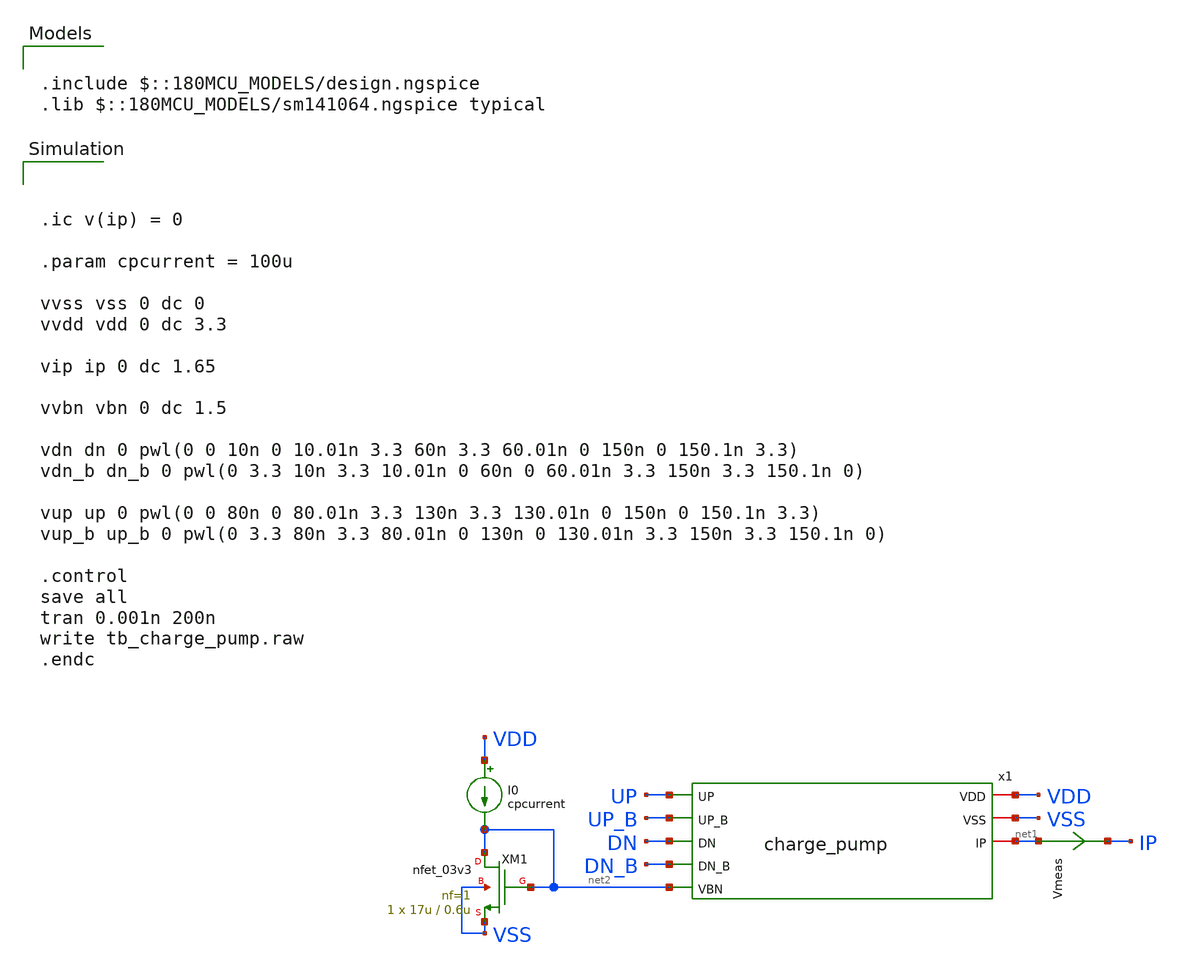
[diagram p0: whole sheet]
** sch_path: designs/libs/tb_analog/tb_charge_pump/tb_charge_pump.sch
**.subckt tb_charge_pump
x1 VDD VSS UP UP_B DN DN_B net2 net1 charge_pump
Vmeas net1 IP 0
.save i(vmeas)
XM1 net2 net2 VSS VSS nfet_03v3 L=0.6u W=17u nf=1 ad='int((nf+1)/2) * W/nf * 0.18u' as='int((nf+2)/2) * W/nf * 0.18u'
+ pd='2*int((nf+1)/2) * (W/nf + 0.18u)' ps='2*int((nf+2)/2) * (W/nf + 0.18u)' nrd='0.18u / W' nrs='0.18u / W'
+ sa=0 sb=0 sd=0 m=1
I0 VDD net2 cpcurrent
**** begin user architecture code



.ic v(ip) = 0

.param cpcurrent = 100u

vvss vss 0 dc 0
vvdd vdd 0 dc 3.3

vip ip 0 dc 1.65

vvbn vbn 0 dc 1.5

vdn dn 0 pwl(0 0 10n 0 10.01n 3.3 60n 3.3 60.01n 0 150n 0 150.1n 3.3)
vdn_b dn_b 0 pwl(0 3.3 10n 3.3 10.01n 0 60n 0 60.01n 3.3 150n 3.3 150.1n 0)

vup up 0 pwl(0 0 80n 0 80.01n 3.3 130n 3.3 130.01n 0 150n 0 150.1n 3.3)
vup_b up_b 0 pwl(0 3.3 80n 3.3 80.01n 0 130n 0 130.01n 3.3 150n 3.3 150.1n 0)

.control
save all
tran 0.001n 200n
write tb_charge_pump.raw
.endc



.include $::180MCU_MODELS/design.ngspice
.lib $::180MCU_MODELS/sm141064.ngspice typical

**** end user architecture code
**.ends

* expanding   symbol:
*+  /foss/designs/synchronos-chipathon-2026/designs/libs/core_analog/charge_pump/charge_pump.sym # of pins=8
** sym_path: designs/libs/core_analog/charge_pump/charge_pump.sym
** sch_path: designs/libs/core_analog/charge_pump/charge_pump.sch
.subckt charge_pump VDD VSS UP UP_B DN DN_B VBN IP
*.iopin VDD
*.iopin VSS
*.ipin UP
*.ipin UP_B
*.ipin DN
*.ipin DN_B
*.ipin VBN
*.iopin IP
XM1 net1 VBN net7 VSS nfet_03v3 L=0.6u W=17u nf=1 ad='int((nf+1)/2) * W/nf * 0.18u' as='int((nf+2)/2) * W/nf * 0.18u'
+ pd='2*int((nf+1)/2) * (W/nf + 0.18u)' ps='2*int((nf+2)/2) * (W/nf + 0.18u)' nrd='0.18u / W' nrs='0.18u / W'
+ sa=0 sb=0 sd=0 m=1
XM2 net2 VBN net6 VSS nfet_03v3 L=0.6u W=17u nf=1 ad='int((nf+1)/2) * W/nf * 0.18u' as='int((nf+2)/2) * W/nf * 0.18u'
+ pd='2*int((nf+1)/2) * (W/nf + 0.18u)' ps='2*int((nf+2)/2) * (W/nf + 0.18u)' nrd='0.18u / W' nrs='0.18u / W'
+ sa=0 sb=0 sd=0 m=1
XM3 net5 DN net1 VSS nfet_03v3 L=0.3u W=1.5u nf=1 ad='int((nf+1)/2) * W/nf * 0.18u' as='int((nf+2)/2) * W/nf * 0.18u'
+ pd='2*int((nf+1)/2) * (W/nf + 0.18u)' ps='2*int((nf+2)/2) * (W/nf + 0.18u)' nrd='0.18u / W' nrs='0.18u / W'
+ sa=0 sb=0 sd=0 m=1
XM4 net3 DN_B net1 VSS nfet_03v3 L=0.3u W=1.5u nf=1 ad='int((nf+1)/2) * W/nf * 0.18u' as='int((nf+2)/2) * W/nf * 0.18u'
+ pd='2*int((nf+1)/2) * (W/nf + 0.18u)' ps='2*int((nf+2)/2) * (W/nf + 0.18u)' nrd='0.18u / W' nrs='0.18u / W'
+ sa=0 sb=0 sd=0 m=1
XM5 net4 UP_B net2 VSS nfet_03v3 L=0.3u W=1.5u nf=1 ad='int((nf+1)/2) * W/nf * 0.18u' as='int((nf+2)/2) * W/nf * 0.18u'
+ pd='2*int((nf+1)/2) * (W/nf + 0.18u)' ps='2*int((nf+2)/2) * (W/nf + 0.18u)' nrd='0.18u / W' nrs='0.18u / W'
+ sa=0 sb=0 sd=0 m=1
XM6 IP UP net2 VSS nfet_03v3 L=0.3u W=1.5u nf=1 ad='int((nf+1)/2) * W/nf * 0.18u' as='int((nf+2)/2) * W/nf * 0.18u'
+ pd='2*int((nf+1)/2) * (W/nf + 0.18u)' ps='2*int((nf+2)/2) * (W/nf + 0.18u)' nrd='0.18u / W' nrs='0.18u / W'
+ sa=0 sb=0 sd=0 m=1
x1 net5 net5 VDD net5 VDD cp_sym_load
x2 net3 net3 VDD net3 VDD cp_sym_load
x3 net4 net4 VDD net4 VDD cp_sym_load
x4 net5 net5 VDD IP VDD cp_sym_load
Vtail net7 VSS 0
.save i(vtail)
Vtail2 net6 VSS 0
.save i(vtail2)
.ends


* expanding   symbol:
*+  /foss/designs/synchronos-chipathon-2026/designs/libs/core_analog/cp_sym_load/cp_sym_load.sym # of pins=5
** sym_path: designs/libs/core_analog/cp_sym_load/cp_sym_load.sym
** sch_path: designs/libs/core_analog/cp_sym_load/cp_sym_load.sch
.subckt cp_sym_load G1 G2 S D VDD
*.ipin G1
*.ipin G2
*.iopin S
*.iopin D
*.iopin VDD
XM1 D G1 S VDD pfet_03v3 L=0.3u W=1.5u nf=1 ad='int((nf+1)/2) * W/nf * 0.18u' as='int((nf+2)/2) * W/nf * 0.18u'
+ pd='2*int((nf+1)/2) * (W/nf + 0.18u)' ps='2*int((nf+2)/2) * (W/nf + 0.18u)' nrd='0.18u / W' nrs='0.18u / W'
+ sa=0 sb=0 sd=0 m=1
XM2 D G2 S VDD pfet_03v3 L=0.3u W=1.5u nf=1 ad='int((nf+1)/2) * W/nf * 0.18u' as='int((nf+2)/2) * W/nf * 0.18u'
+ pd='2*int((nf+1)/2) * (W/nf + 0.18u)' ps='2*int((nf+2)/2) * (W/nf + 0.18u)' nrd='0.18u / W' nrs='0.18u / W'
+ sa=0 sb=0 sd=0 m=1
.ends

.end
